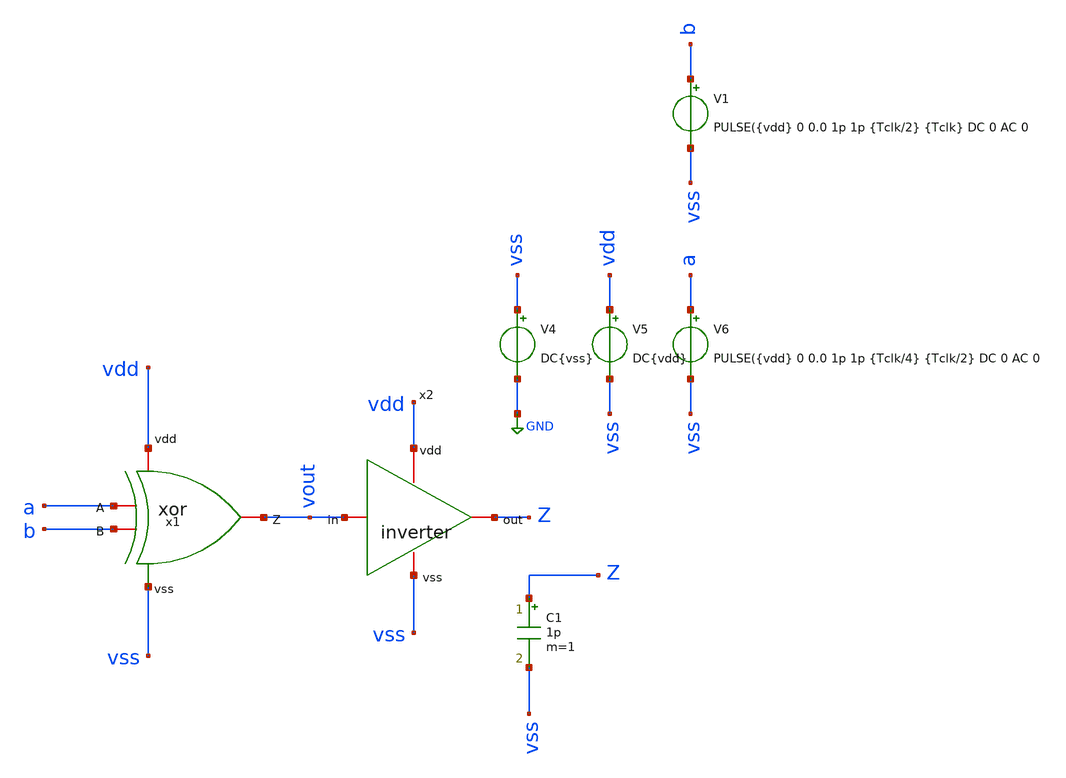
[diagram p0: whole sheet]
** sch_path: tstbnch/xor_test.sch
**.subckt xor_test
V4 vss GND DC{vss}
V5 vdd vss DC{vdd}
V6 a vss PULSE({vdd} 0 0.0 1p 1p {Tclk/4} {Tclk/2} DC 0 AC 0
C1 Z vss 1p m=1
V1 b vss PULSE({vdd} 0 0.0 1p 1p {Tclk/2} {Tclk} DC 0 AC 0
x2 vdd vout Z vss inverter
x1 vdd a b vout vss xor
**** begin user architecture code


* Circuit Parameters
.param vdd = 1.8
.param vss = 0.0
.param Tclk = 20n
.options TEMP = 65.0
* Include Models
.lib /foss/pdks/sky130A/libs.tech/ngspice/sky130.lib.spice TT
* OP Parameters & Singals to save
.save all



*Simulations

.control

tran 0.01u 100n
setplot tran1
plot v(a) v(b)+2 v(vout)+4
reset

dc a 0 1.8 0.01
dc b 0 1.8 0.01
setplot dc
plot vin vout ylabel vout xlabel vin

set filetype = ascii
write dcsweep.raw
.endc
.end


**** end user architecture code
**.ends
.GLOBAL GND
.end
